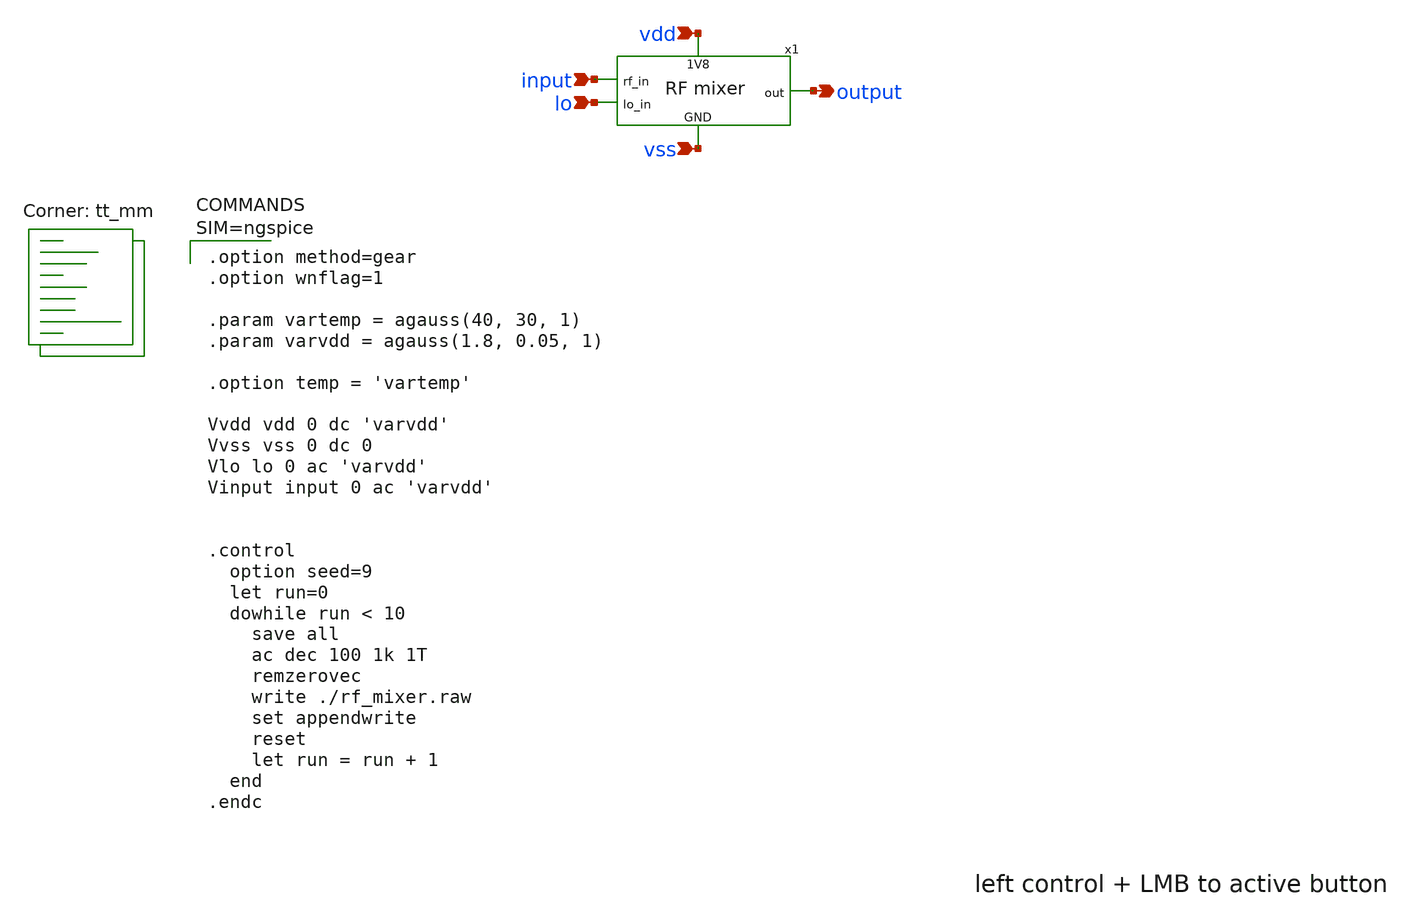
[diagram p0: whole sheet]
** sch_path: tests/rf_mixer.sch
**.subckt rf_mixer input output vdd vss lo
*.ipin input
*.opin output
*.ipin vdd
*.ipin vss
*.ipin lo
x1 input lo vdd output vss rf_mixer
**** begin user architecture code
.lib $::SKYWATER_MODELS/sky130.lib.spice tt_mm


.option method=gear
.option wnflag=1

.param vartemp = agauss(40, 30, 1)
.param varvdd = agauss(1.8, 0.05, 1)

.option temp = 'vartemp'

Vvdd vdd 0 dc 'varvdd'
Vvss vss 0 dc 0
Vlo lo 0 ac 'varvdd'
Vinput input 0 ac 'varvdd'


.control
  option seed=9
  let run=0
  dowhile run < 10
    save all
    ac dec 100 1k 1T
    remzerovec
    write ./rf_mixer.raw
    set appendwrite
    reset
    let run = run + 1
  end
.endc


**** end user architecture code
**.ends

* expanding   symbol:  ./rf_mixer.sym # of pins=5
** sym_path: schematic/rf_mixer.sym
** sch_path: schematic/rf_mixer.sch
.subckt rf_mixer rf_in lo_in 1V8 out GND
*.ipin rf_in
*.opin out
*.ipin GND
*.ipin 1V8
*.ipin lo_in
* noconn 1V8
* noconn GND
* noconn lo_in
R1 out rf_in 0 m=1
.ends

.end
